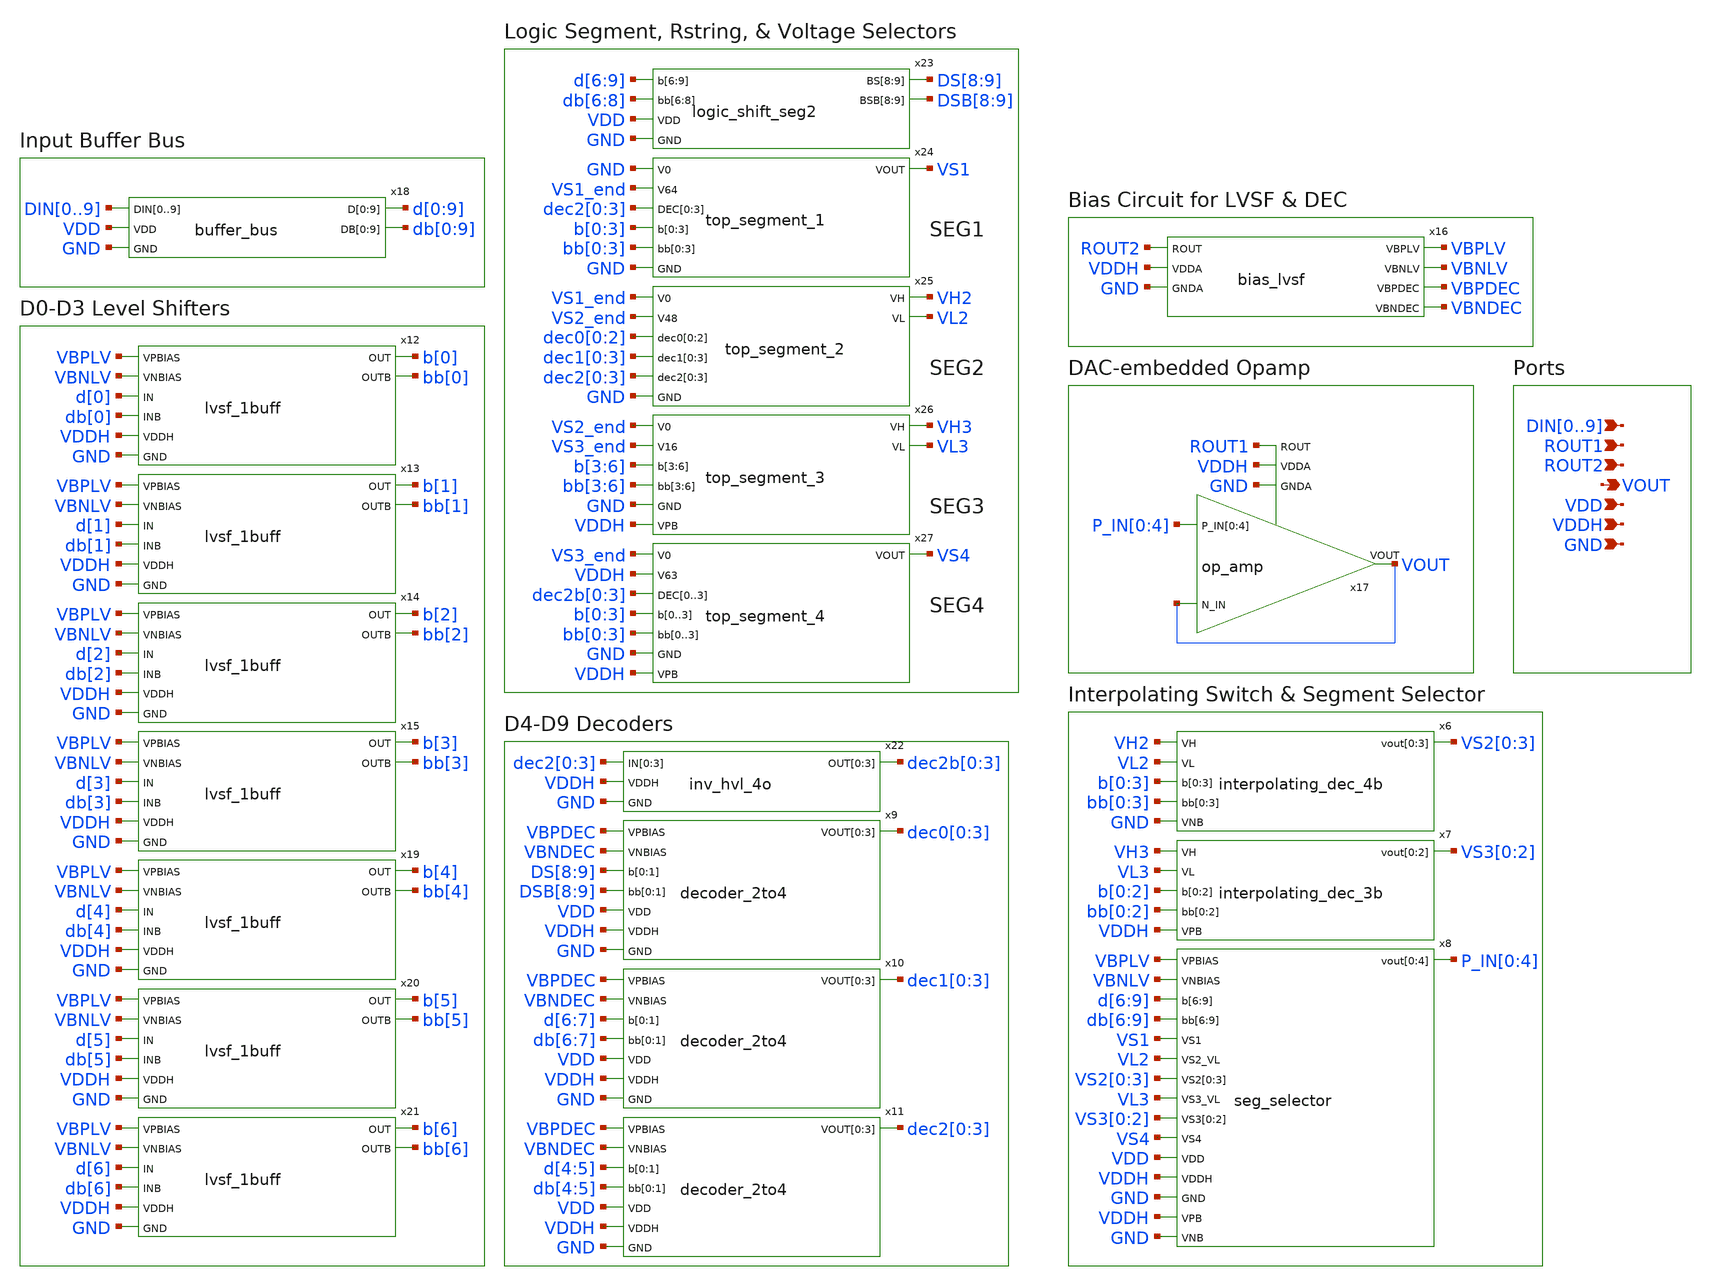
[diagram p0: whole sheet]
** sch_path: xschem/DAC_10b_top.sch
**.subckt DAC_10b_top VOUT GND DIN0,DIN1,DIN2,DIN3,DIN4,DIN5,DIN6,DIN7,DIN8,DIN9 VDD VDDH ROUT1
*+ ROUT2
*.opin VOUT
*.ipin GND
*.ipin DIN0,DIN1,DIN2,DIN3,DIN4,DIN5,DIN6,DIN7,DIN8,DIN9
*.ipin VDD
*.ipin VDDH
*.ipin ROUT1
*.ipin ROUT2
x6 VH2 VL2 b[0] b[1] b[2] b[3] bb[0] bb[1] bb[2] bb[3] VS2[0] VS2[1] VS2[2] VS2[3] GND
+ interpolating_dec_4b
x7 VH3 VL3 b[0] b[1] b[2] bb[0] bb[1] bb[2] VS3[0] VS3[1] VS3[2] VDDH interpolating_dec_3b
x8 VBPLV VBNLV d[6] d[7] d[8] d[9] db[6] db[7] db[8] db[9] VS1 VL2 VS2[0] VS2[1] VS2[2] VS2[3] VL3
+ VS3[0] VS3[1] VS3[2] VS4 P_IN[0] P_IN[1] P_IN[2] P_IN[3] P_IN[4] VDD VDDH GND VDDH GND seg_selector
x9 VBPDEC VBNDEC DS[8] DS[9] DSB[8] DSB[9] dec0[0] dec0[1] dec0[2] dec0[3] VDD VDDH GND decoder_2to4
x10 VBPDEC VBNDEC d[6] d[7] db[6] db[7] dec1[0] dec1[1] dec1[2] dec1[3] VDD VDDH GND decoder_2to4
x11 VBPDEC VBNDEC d[4] d[5] db[4] db[5] dec2[0] dec2[1] dec2[2] dec2[3] VDD VDDH GND decoder_2to4
x12 VBPLV VBNLV d[0] db[0] b[0] bb[0] VDDH GND lvsf_1buff
x13 VBPLV VBNLV d[1] db[1] b[1] bb[1] VDDH GND lvsf_1buff
x14 VBPLV VBNLV d[2] db[2] b[2] bb[2] VDDH GND lvsf_1buff
x15 VBPLV VBNLV d[3] db[3] b[3] bb[3] VDDH GND lvsf_1buff
x17 P_IN[0] P_IN[1] P_IN[2] P_IN[3] P_IN[4] VOUT VOUT ROUT1 VDDH GND op_amp
x16 ROUT2 VBPLV VBNLV VBPDEC VBNDEC VDDH GND bias_lvsf
x18 DIN0 DIN1 DIN2 DIN3 DIN4 DIN5 DIN6 DIN7 DIN8 DIN9 d[0] d[1] d[2] d[3] d[4] d[5] d[6] d[7] d[8]
+ d[9] db[0] db[1] db[2] db[3] db[4] db[5] db[6] db[7] db[8] db[9] VDD GND buffer_bus
x19 VBPLV VBNLV d[4] db[4] b[4] bb[4] VDDH GND lvsf_1buff
x20 VBPLV VBNLV d[5] db[5] b[5] bb[5] VDDH GND lvsf_1buff
x21 VBPLV VBNLV d[6] db[6] b[6] bb[6] VDDH GND lvsf_1buff
x22 dec2[0] dec2[1] dec2[2] dec2[3] dec2b[0] dec2b[1] dec2b[2] dec2b[3] VDDH GND inv_hvl_4o
x23 d[6] d[7] d[8] d[9] db[6] db[7] db[8] DS[8] DS[9] DSB[8] DSB[9] VDD GND logic_shift_seg2
x24 GND VS1_end dec2[0] dec2[1] dec2[2] dec2[3] b[0] b[1] b[2] b[3] bb[0] bb[1] bb[2] bb[3] VS1 GND
+ top_segment_1
x25 VS1_end VS2_end dec0[0] dec0[1] dec0[2] dec1[0] dec1[1] dec1[2] dec1[3] dec2[0] dec2[1] dec2[2]
+ dec2[3] VH2 VL2 GND top_segment_2
x26 VS2_end VS3_end b[3] b[4] b[5] b[6] bb[3] bb[4] bb[5] bb[6] VH3 VL3 GND VDDH top_segment_3
x27 VS3_end VDDH dec2b[0] dec2b[1] dec2b[2] dec2b[3] b[0] b[1] b[2] b[3] bb[0] bb[1] bb[2] bb[3] VS4
+ GND VDDH top_segment_4
**.ends
.end
